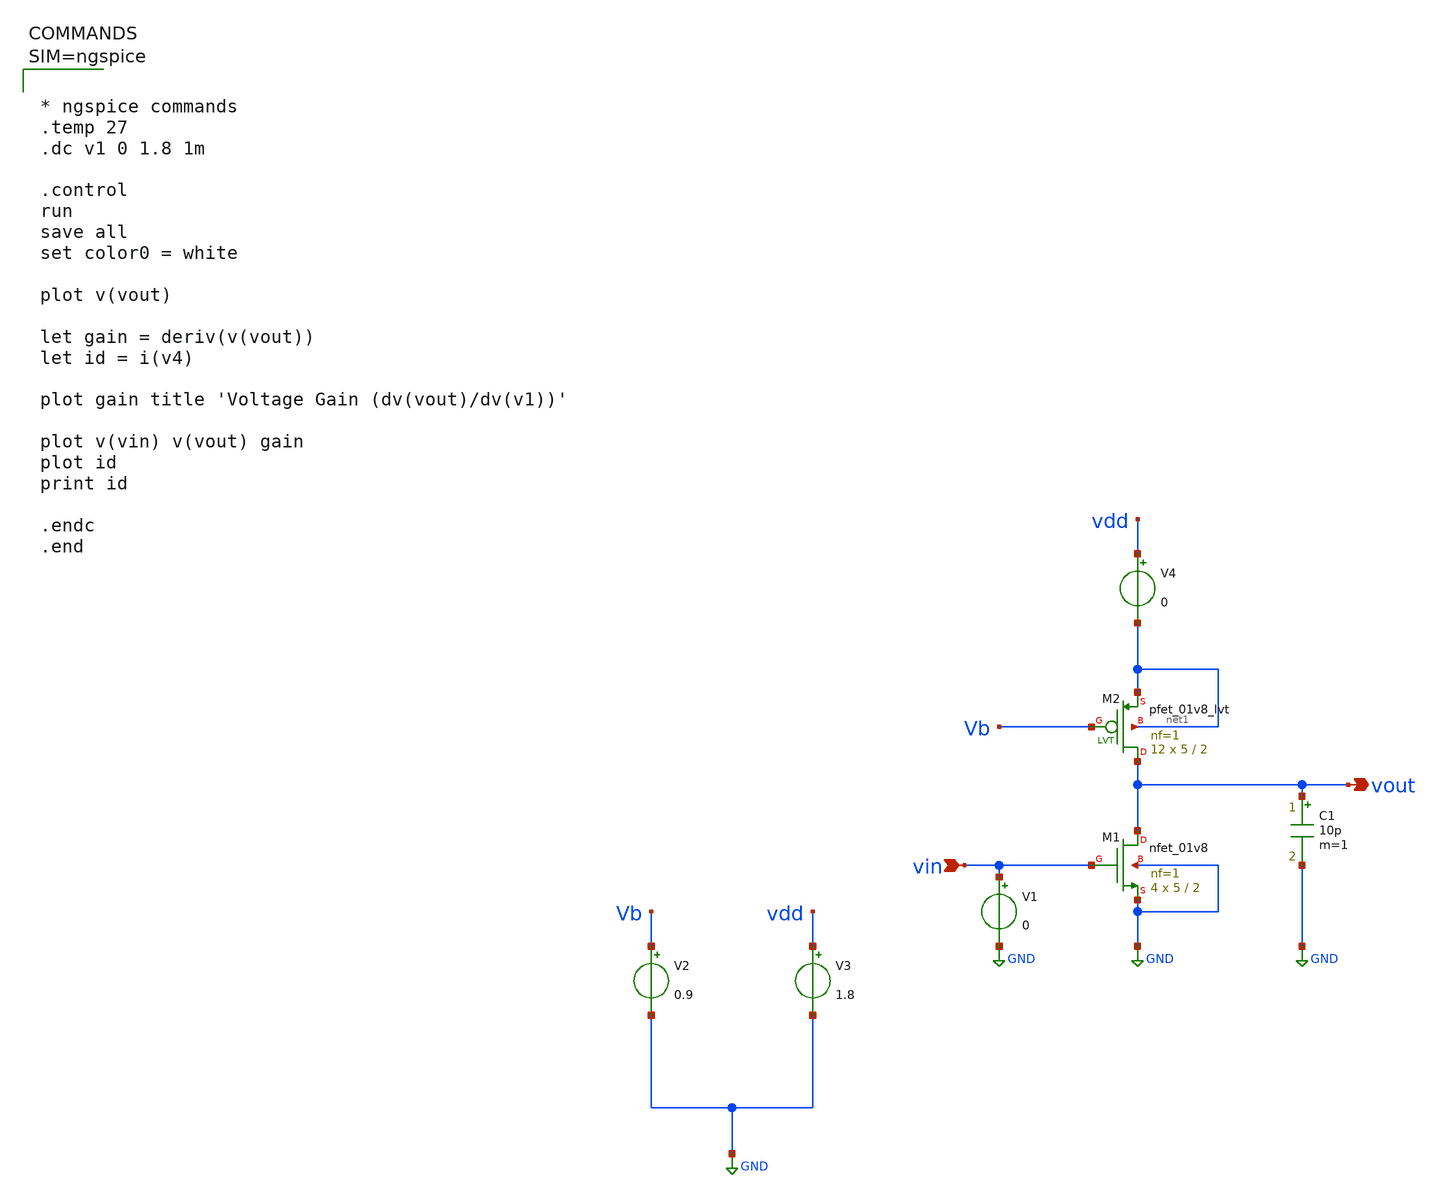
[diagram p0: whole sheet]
** sch_path: sch/NMOS_pmos_load_amp.sch
**.subckt NMOS_pmos_load_amp vin vout
*.ipin vin
*.opin vout
C1 vout GND 10p m=1
V1 vin GND 0
V2 Vb GND 0.9
V3 vdd GND 1.8
XM2 vout Vb net1 net1 sky130_fd_pr__pfet_01v8_lvt L=2 W=5 nf=1 ad='int((1 + 1)/2) * 5 / 1 * 0.29' as='int((1 + 2)/2) * 5 / 1 * 0.29'
+ pd='2*int((1 + 1)/2) * (5 / 1 + 0.29)' ps='2*int((1 + 2)/2) * (5 / 1 + 0.29)' nrd='0.29 / 5 ' nrs='0.29 / 5 '
+ sa=0 sb=0 sd=0 mult=12 m=12
XM1 vout vin GND GND sky130_fd_pr__nfet_01v8 L=2 W=5 nf=1 ad='int((1 + 1)/2) * 5 / 1 * 0.29' as='int((1 + 2)/2) * 5 / 1 * 0.29'
+ pd='2*int((1 + 1)/2) * (5 / 1 + 0.29)' ps='2*int((1 + 2)/2) * (5 / 1 + 0.29)' nrd='0.29 / 5 ' nrs='0.29 / 5 '
+ sa=0 sb=0 sd=0 mult=4 m=4
V4 vdd net1 0
**** begin user architecture code

** opencircuitdesign pdks install
.lib $::SKYWATER_MODELS/sky130.lib.spice tt




* ngspice commands
.temp 27
.dc v1 0 1.8 1m

.control
run
save all
set color0 = white

plot v(vout)

let gain = deriv(v(vout))
let id = i(v4)

plot gain title 'Voltage Gain (dv(vout)/dv(v1))'

plot v(vin) v(vout) gain
plot id
print id

.endc
.end



**** end user architecture code
**.ends
.GLOBAL GND
.end
